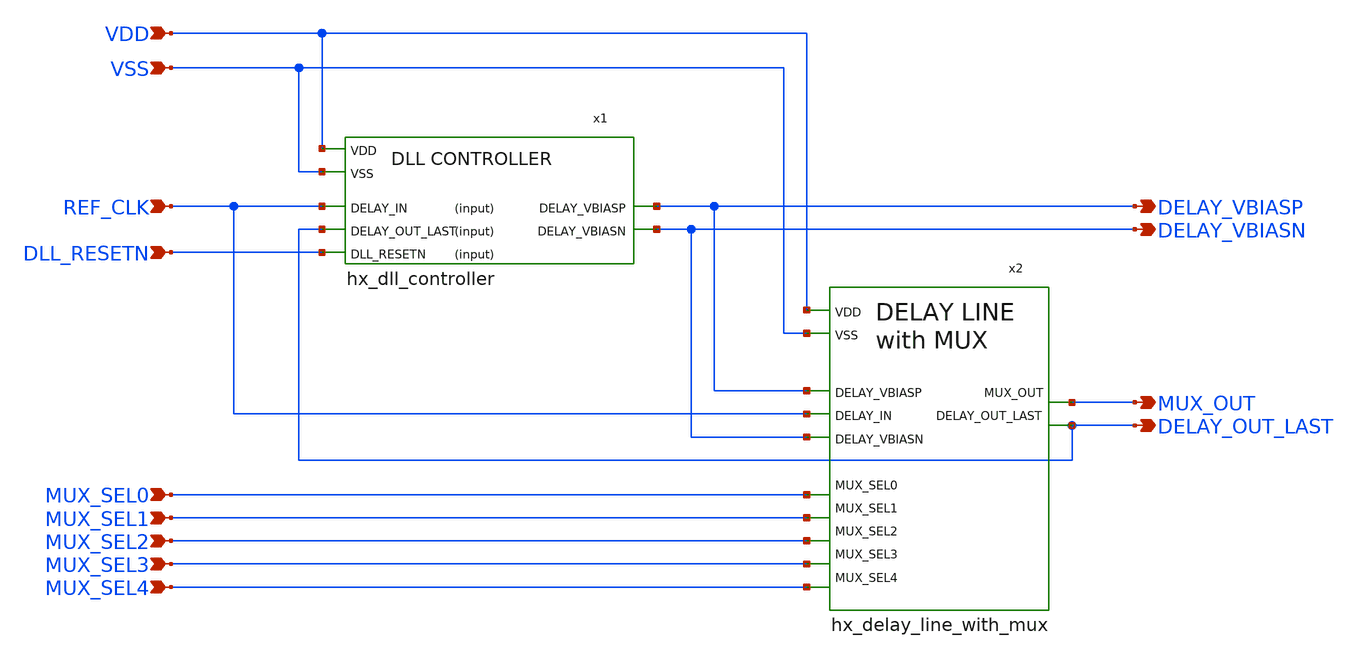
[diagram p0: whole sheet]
** sch_path: schematics/hx_delay_line_with_mux_dll.sch
**.subckt hx_delay_line_with_mux_dll VDD VSS MUX_OUT REF_CLK DLL_RESETN MUX_SEL0 MUX_SEL1 MUX_SEL2
*+ MUX_SEL3 MUX_SEL4 DELAY_VBIASN DELAY_VBIASP DELAY_OUT_LAST
*.ipin VDD
*.ipin VSS
*.opin MUX_OUT
*.ipin REF_CLK
*.ipin DLL_RESETN
*.ipin MUX_SEL0
*.ipin MUX_SEL1
*.ipin MUX_SEL2
*.ipin MUX_SEL3
*.ipin MUX_SEL4
*.opin DELAY_VBIASN
*.opin DELAY_VBIASP
*.opin DELAY_OUT_LAST
x1 VDD DLL_RESETN DELAY_OUT_LAST VSS REF_CLK DELAY_VBIASN DELAY_VBIASP hx_dll_controller
x2 DELAY_OUT_LAST VSS VDD REF_CLK MUX_SEL0 MUX_SEL1 MUX_OUT MUX_SEL4 MUX_SEL2 MUX_SEL3 DELAY_VBIASN
+ DELAY_VBIASP hx_delay_line_with_mux
**.ends
.end
